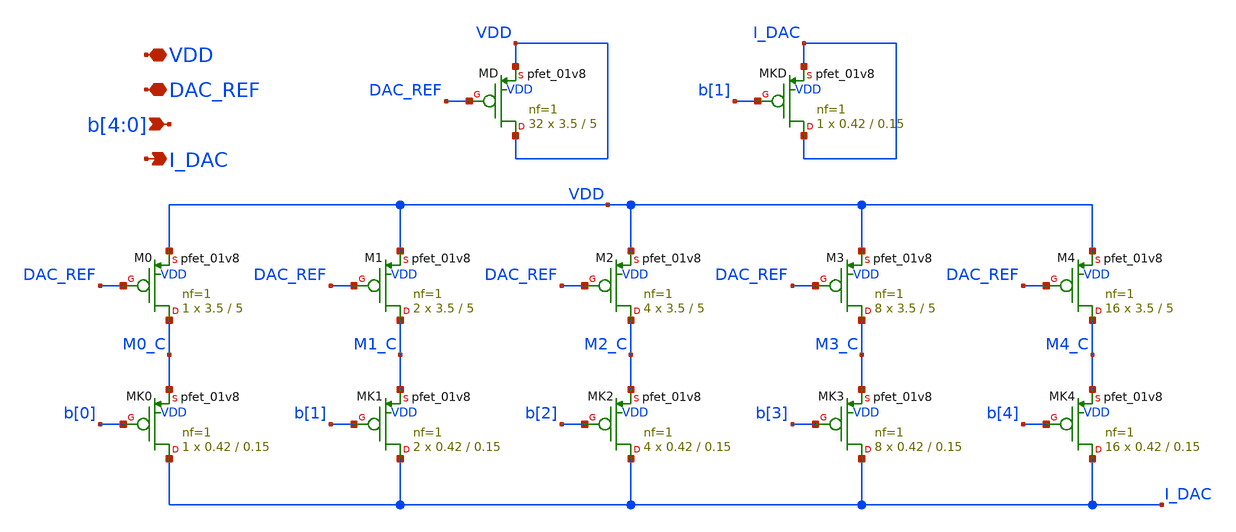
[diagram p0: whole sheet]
** sch_path: designs_backup/designs/lab2/xschem/DAC_CORE_5bit.sch
**.subckt DAC_CORE_5bit DAC_REF b[4],b[3],b[2],b[1],b[0] VDD I_DAC
*.iopin DAC_REF
*.ipin b[4],b[3],b[2],b[1],b[0]
*.iopin VDD
*.opin I_DAC
XM1 M1_C DAC_REF VDD VDD sky130_fd_pr__pfet_01v8 L=5 W=3.5 nf=1 ad='int((1 + 1)/2) * 3.5 / 1 * 0.29'
+ as='int((1 + 2)/2) * 3.5 / 1 * 0.29' pd='2*int((1 + 1)/2) * (3.5 / 1 + 0.29)' ps='2*int((1 + 2)/2) * (3.5 / 1 + 0.29)'
+ nrd='0.29 / 3.5 ' nrs='0.29 / 3.5 ' sa=0 sb=0 sd=0 mult=2 m=2
XM2 M2_C DAC_REF VDD VDD sky130_fd_pr__pfet_01v8 L=5 W=3.5 nf=1 ad='int((1 + 1)/2) * 3.5 / 1 * 0.29'
+ as='int((1 + 2)/2) * 3.5 / 1 * 0.29' pd='2*int((1 + 1)/2) * (3.5 / 1 + 0.29)' ps='2*int((1 + 2)/2) * (3.5 / 1 + 0.29)'
+ nrd='0.29 / 3.5 ' nrs='0.29 / 3.5 ' sa=0 sb=0 sd=0 mult=4 m=4
XM3 M3_C DAC_REF VDD VDD sky130_fd_pr__pfet_01v8 L=5 W=3.5 nf=1 ad='int((1 + 1)/2) * 3.5 / 1 * 0.29'
+ as='int((1 + 2)/2) * 3.5 / 1 * 0.29' pd='2*int((1 + 1)/2) * (3.5 / 1 + 0.29)' ps='2*int((1 + 2)/2) * (3.5 / 1 + 0.29)'
+ nrd='0.29 / 3.5 ' nrs='0.29 / 3.5 ' sa=0 sb=0 sd=0 mult=8 m=8
XM4 M4_C DAC_REF VDD VDD sky130_fd_pr__pfet_01v8 L=5 W=3.5 nf=1 ad='int((1 + 1)/2) * 3.5 / 1 * 0.29'
+ as='int((1 + 2)/2) * 3.5 / 1 * 0.29' pd='2*int((1 + 1)/2) * (3.5 / 1 + 0.29)' ps='2*int((1 + 2)/2) * (3.5 / 1 + 0.29)'
+ nrd='0.29 / 3.5 ' nrs='0.29 / 3.5 ' sa=0 sb=0 sd=0 mult=16 m=16
XM0 M0_C DAC_REF VDD VDD sky130_fd_pr__pfet_01v8 L=5 W=3.5 nf=1 ad='int((1 + 1)/2) * 3.5 / 1 * 0.29'
+ as='int((1 + 2)/2) * 3.5 / 1 * 0.29' pd='2*int((1 + 1)/2) * (3.5 / 1 + 0.29)' ps='2*int((1 + 2)/2) * (3.5 / 1 + 0.29)'
+ nrd='0.29 / 3.5 ' nrs='0.29 / 3.5 ' sa=0 sb=0 sd=0 mult=1 m=1
XMK0 I_DAC b[0] M0_C VDD sky130_fd_pr__pfet_01v8 L=0.15 W=0.42 nf=1 ad='int((1 + 1)/2) * 0.42 / 1 * 0.29'
+ as='int((1 + 2)/2) * 0.42 / 1 * 0.29' pd='2*int((1 + 1)/2) * (0.42 / 1 + 0.29)' ps='2*int((1 + 2)/2) * (0.42 / 1 + 0.29)'
+ nrd='0.29 / 0.42 ' nrs='0.29 / 0.42 ' sa=0 sb=0 sd=0 mult=1 m=1
XMK1 I_DAC b[1] M1_C VDD sky130_fd_pr__pfet_01v8 L=0.15 W=0.42 nf=1 ad='int((1 + 1)/2) * 0.42 / 1 * 0.29'
+ as='int((1 + 2)/2) * 0.42 / 1 * 0.29' pd='2*int((1 + 1)/2) * (0.42 / 1 + 0.29)' ps='2*int((1 + 2)/2) * (0.42 / 1 + 0.29)'
+ nrd='0.29 / 0.42 ' nrs='0.29 / 0.42 ' sa=0 sb=0 sd=0 mult=2 m=2
XMK2 I_DAC b[2] M2_C VDD sky130_fd_pr__pfet_01v8 L=0.15 W=0.42 nf=1 ad='int((1 + 1)/2) * 0.42 / 1 * 0.29'
+ as='int((1 + 2)/2) * 0.42 / 1 * 0.29' pd='2*int((1 + 1)/2) * (0.42 / 1 + 0.29)' ps='2*int((1 + 2)/2) * (0.42 / 1 + 0.29)'
+ nrd='0.29 / 0.42 ' nrs='0.29 / 0.42 ' sa=0 sb=0 sd=0 mult=4 m=4
XMK3 I_DAC b[3] M3_C VDD sky130_fd_pr__pfet_01v8 L=0.15 W=0.42 nf=1 ad='int((1 + 1)/2) * 0.42 / 1 * 0.29'
+ as='int((1 + 2)/2) * 0.42 / 1 * 0.29' pd='2*int((1 + 1)/2) * (0.42 / 1 + 0.29)' ps='2*int((1 + 2)/2) * (0.42 / 1 + 0.29)'
+ nrd='0.29 / 0.42 ' nrs='0.29 / 0.42 ' sa=0 sb=0 sd=0 mult=8 m=8
XMK4 I_DAC b[4] M4_C VDD sky130_fd_pr__pfet_01v8 L=0.15 W=0.42 nf=1 ad='int((1 + 1)/2) * 0.42 / 1 * 0.29'
+ as='int((1 + 2)/2) * 0.42 / 1 * 0.29' pd='2*int((1 + 1)/2) * (0.42 / 1 + 0.29)' ps='2*int((1 + 2)/2) * (0.42 / 1 + 0.29)'
+ nrd='0.29 / 0.42 ' nrs='0.29 / 0.42 ' sa=0 sb=0 sd=0 mult=16 m=16
XMD VDD DAC_REF VDD VDD sky130_fd_pr__pfet_01v8 L=5 W=3.5 nf=1 ad='int((1 + 1)/2) * 3.5 / 1 * 0.29' as='int((1 + 2)/2) * 3.5 / 1 * 0.29'
+ pd='2*int((1 + 1)/2) * (3.5 / 1 + 0.29)' ps='2*int((1 + 2)/2) * (3.5 / 1 + 0.29)' nrd='0.29 / 3.5 ' nrs='0.29 / 3.5 '
+ sa=0 sb=0 sd=0 mult=32 m=32
XMKD I_DAC b[1] I_DAC VDD sky130_fd_pr__pfet_01v8 L=0.15 W=0.42 nf=1 ad='int((1 + 1)/2) * 0.42 / 1 * 0.29'
+ as='int((1 + 2)/2) * 0.42 / 1 * 0.29' pd='2*int((1 + 1)/2) * (0.42 / 1 + 0.29)' ps='2*int((1 + 2)/2) * (0.42 / 1 + 0.29)'
+ nrd='0.29 / 0.42 ' nrs='0.29 / 0.42 ' sa=0 sb=0 sd=0 mult=1 m=1
**.ends
.end
